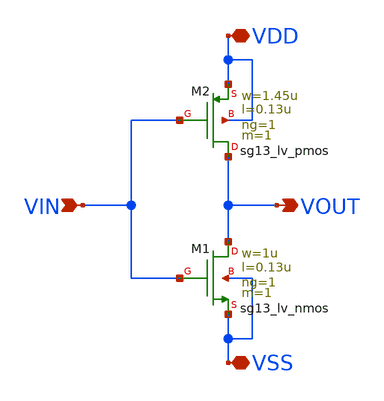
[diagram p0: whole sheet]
** sch_path: inv.sch
**.subckt inv VDD VSS VOUT VIN
*.iopin VDD
*.iopin VSS
*.opin VOUT
*.ipin VIN
XM2 VOUT VIN VDD VDD sg13_lv_pmos w=1.45u l=0.13u ng=1 m=1 mm_ok=1
XM1 VOUT VIN VSS VSS sg13_lv_nmos w=1u l=0.13u ng=1 m=1 mm_ok=1
**.ends
.end
